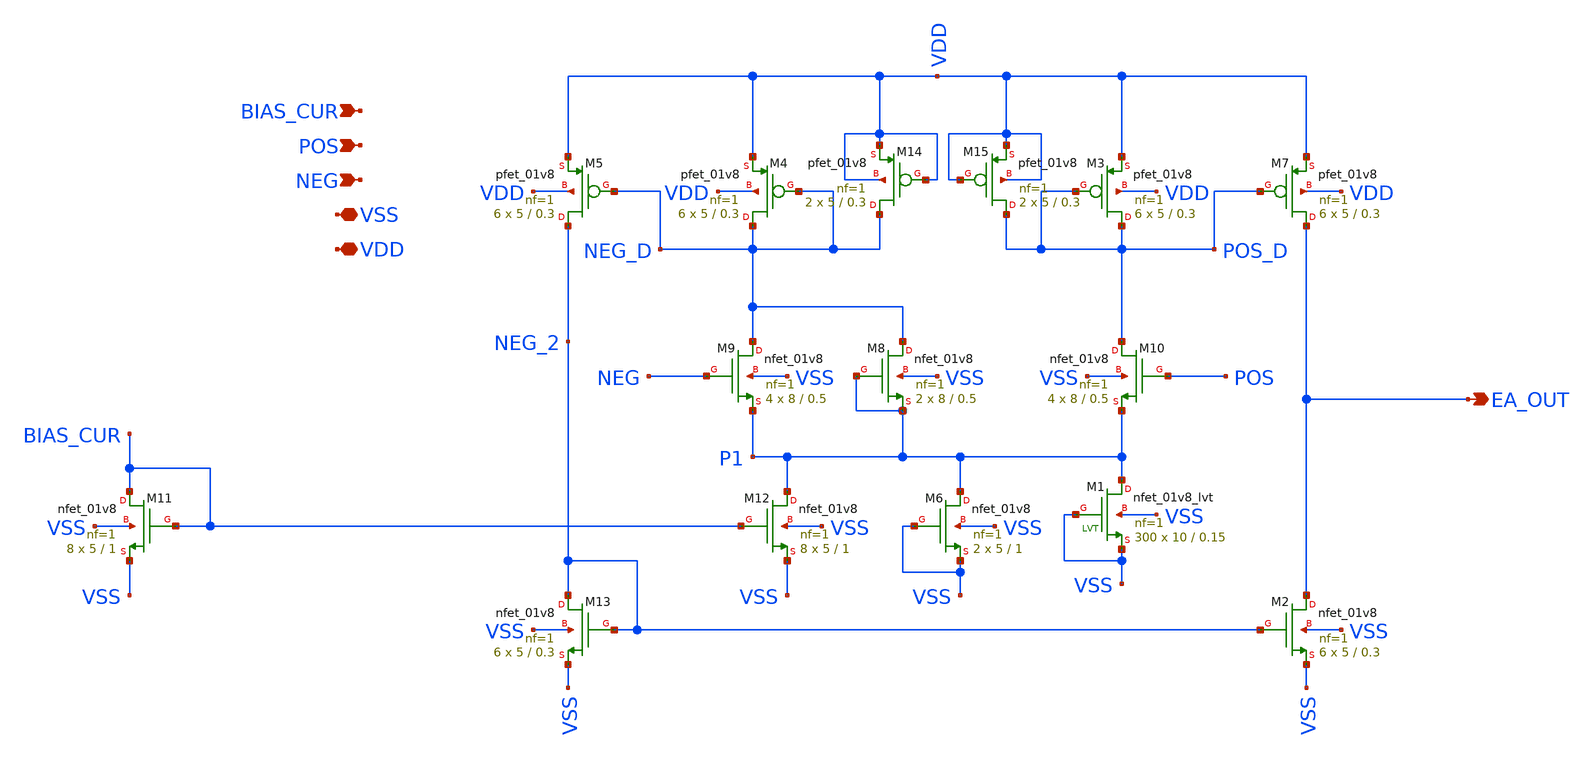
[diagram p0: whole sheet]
** sch_path: xschem/opamp.sch
**.subckt opamp POS NEG VDD VSS BIAS_CUR EA_OUT
*.ipin POS
*.ipin NEG
*.iopin VDD
*.iopin VSS
*.ipin BIAS_CUR
*.opin EA_OUT
XM3 POS_D POS_D VDD VDD sky130_fd_pr__pfet_01v8 L=0.3 W=5 nf=1 ad='int((nf+1)/2) * W/nf * 0.29' as='int((nf+2)/2) * W/nf * 0.29'
+ pd='2*int((nf+1)/2) * (W/nf + 0.29)' ps='2*int((nf+2)/2) * (W/nf + 0.29)' nrd='0.29 / W' nrs='0.29 / W'
+ sa=0 sb=0 sd=0 mult=6 m=6
XM4 NEG_D NEG_D VDD VDD sky130_fd_pr__pfet_01v8 L=0.3 W=5 nf=1 ad='int((nf+1)/2) * W/nf * 0.29' as='int((nf+2)/2) * W/nf * 0.29'
+ pd='2*int((nf+1)/2) * (W/nf + 0.29)' ps='2*int((nf+2)/2) * (W/nf + 0.29)' nrd='0.29 / W' nrs='0.29 / W'
+ sa=0 sb=0 sd=0 mult=6 m=6
XM5 NEG_2 NEG_D VDD VDD sky130_fd_pr__pfet_01v8 L=0.3 W=5 nf=1 ad='int((nf+1)/2) * W/nf * 0.29' as='int((nf+2)/2) * W/nf * 0.29'
+ pd='2*int((nf+1)/2) * (W/nf + 0.29)' ps='2*int((nf+2)/2) * (W/nf + 0.29)' nrd='0.29 / W' nrs='0.29 / W'
+ sa=0 sb=0 sd=0 mult=6 m=6
XM7 EA_OUT POS_D VDD VDD sky130_fd_pr__pfet_01v8 L=0.3 W=5 nf=1 ad='int((nf+1)/2) * W/nf * 0.29' as='int((nf+2)/2) * W/nf * 0.29'
+ pd='2*int((nf+1)/2) * (W/nf + 0.29)' ps='2*int((nf+2)/2) * (W/nf + 0.29)' nrd='0.29 / W' nrs='0.29 / W'
+ sa=0 sb=0 sd=0 mult=6 m=6
XM9 NEG_D NEG P1 VSS sky130_fd_pr__nfet_01v8 L=0.5 W=8 nf=1 ad='int((nf+1)/2) * W/nf * 0.29' as='int((nf+2)/2) * W/nf * 0.29'
+ pd='2*int((nf+1)/2) * (W/nf + 0.29)' ps='2*int((nf+2)/2) * (W/nf + 0.29)' nrd='0.29 / W' nrs='0.29 / W'
+ sa=0 sb=0 sd=0 mult=4 m=4
XM10 POS_D POS P1 VSS sky130_fd_pr__nfet_01v8 L=0.5 W=8 nf=1 ad='int((nf+1)/2) * W/nf * 0.29' as='int((nf+2)/2) * W/nf * 0.29'
+ pd='2*int((nf+1)/2) * (W/nf + 0.29)' ps='2*int((nf+2)/2) * (W/nf + 0.29)' nrd='0.29 / W' nrs='0.29 / W'
+ sa=0 sb=0 sd=0 mult=4 m=4
XM11 BIAS_CUR BIAS_CUR VSS VSS sky130_fd_pr__nfet_01v8 L=1 W=5 nf=1 ad='int((nf+1)/2) * W/nf * 0.29'
+ as='int((nf+2)/2) * W/nf * 0.29' pd='2*int((nf+1)/2) * (W/nf + 0.29)' ps='2*int((nf+2)/2) * (W/nf + 0.29)'
+ nrd='0.29 / W' nrs='0.29 / W' sa=0 sb=0 sd=0 mult=8 m=8
XM12 P1 BIAS_CUR VSS VSS sky130_fd_pr__nfet_01v8 L=1 W=5 nf=1 ad='int((nf+1)/2) * W/nf * 0.29' as='int((nf+2)/2) * W/nf * 0.29'
+ pd='2*int((nf+1)/2) * (W/nf + 0.29)' ps='2*int((nf+2)/2) * (W/nf + 0.29)' nrd='0.29 / W' nrs='0.29 / W'
+ sa=0 sb=0 sd=0 mult=8 m=8
XM13 NEG_2 NEG_2 VSS VSS sky130_fd_pr__nfet_01v8 L=0.3 W=5 nf=1 ad='int((nf+1)/2) * W/nf * 0.29' as='int((nf+2)/2) * W/nf * 0.29'
+ pd='2*int((nf+1)/2) * (W/nf + 0.29)' ps='2*int((nf+2)/2) * (W/nf + 0.29)' nrd='0.29 / W' nrs='0.29 / W'
+ sa=0 sb=0 sd=0 mult=6 m=6
XM1 P1 VSS VSS VSS sky130_fd_pr__nfet_01v8_lvt L=0.15 W=10 nf=1 ad='int((nf+1)/2) * W/nf * 0.29' as='int((nf+2)/2) * W/nf * 0.29'
+ pd='2*int((nf+1)/2) * (W/nf + 0.29)' ps='2*int((nf+2)/2) * (W/nf + 0.29)' nrd='0.29 / W' nrs='0.29 / W'
+ sa=0 sb=0 sd=0 mult=300 m=300
XM2 EA_OUT NEG_2 VSS VSS sky130_fd_pr__nfet_01v8 L=0.3 W=5 nf=1 ad='int((nf+1)/2) * W/nf * 0.29' as='int((nf+2)/2) * W/nf * 0.29'
+ pd='2*int((nf+1)/2) * (W/nf + 0.29)' ps='2*int((nf+2)/2) * (W/nf + 0.29)' nrd='0.29 / W' nrs='0.29 / W'
+ sa=0 sb=0 sd=0 mult=6 m=6
XM6 P1 VSS VSS VSS sky130_fd_pr__nfet_01v8 L=1 W=5 nf=1 ad='int((nf+1)/2) * W/nf * 0.29' as='int((nf+2)/2) * W/nf * 0.29'
+ pd='2*int((nf+1)/2) * (W/nf + 0.29)' ps='2*int((nf+2)/2) * (W/nf + 0.29)' nrd='0.29 / W' nrs='0.29 / W'
+ sa=0 sb=0 sd=0 mult=2 m=2
XM8 NEG_D P1 P1 VSS sky130_fd_pr__nfet_01v8 L=0.5 W=8 nf=1 ad='int((nf+1)/2) * W/nf * 0.29' as='int((nf+2)/2) * W/nf * 0.29'
+ pd='2*int((nf+1)/2) * (W/nf + 0.29)' ps='2*int((nf+2)/2) * (W/nf + 0.29)' nrd='0.29 / W' nrs='0.29 / W'
+ sa=0 sb=0 sd=0 mult=2 m=2
XM14 NEG_D VDD VDD VDD sky130_fd_pr__pfet_01v8 L=0.3 W=5 nf=1 ad='int((nf+1)/2) * W/nf * 0.29' as='int((nf+2)/2) * W/nf * 0.29'
+ pd='2*int((nf+1)/2) * (W/nf + 0.29)' ps='2*int((nf+2)/2) * (W/nf + 0.29)' nrd='0.29 / W' nrs='0.29 / W'
+ sa=0 sb=0 sd=0 mult=2 m=2
XM15 POS_D VDD VDD VDD sky130_fd_pr__pfet_01v8 L=0.3 W=5 nf=1 ad='int((nf+1)/2) * W/nf * 0.29' as='int((nf+2)/2) * W/nf * 0.29'
+ pd='2*int((nf+1)/2) * (W/nf + 0.29)' ps='2*int((nf+2)/2) * (W/nf + 0.29)' nrd='0.29 / W' nrs='0.29 / W'
+ sa=0 sb=0 sd=0 mult=2 m=2
**.ends
.end
